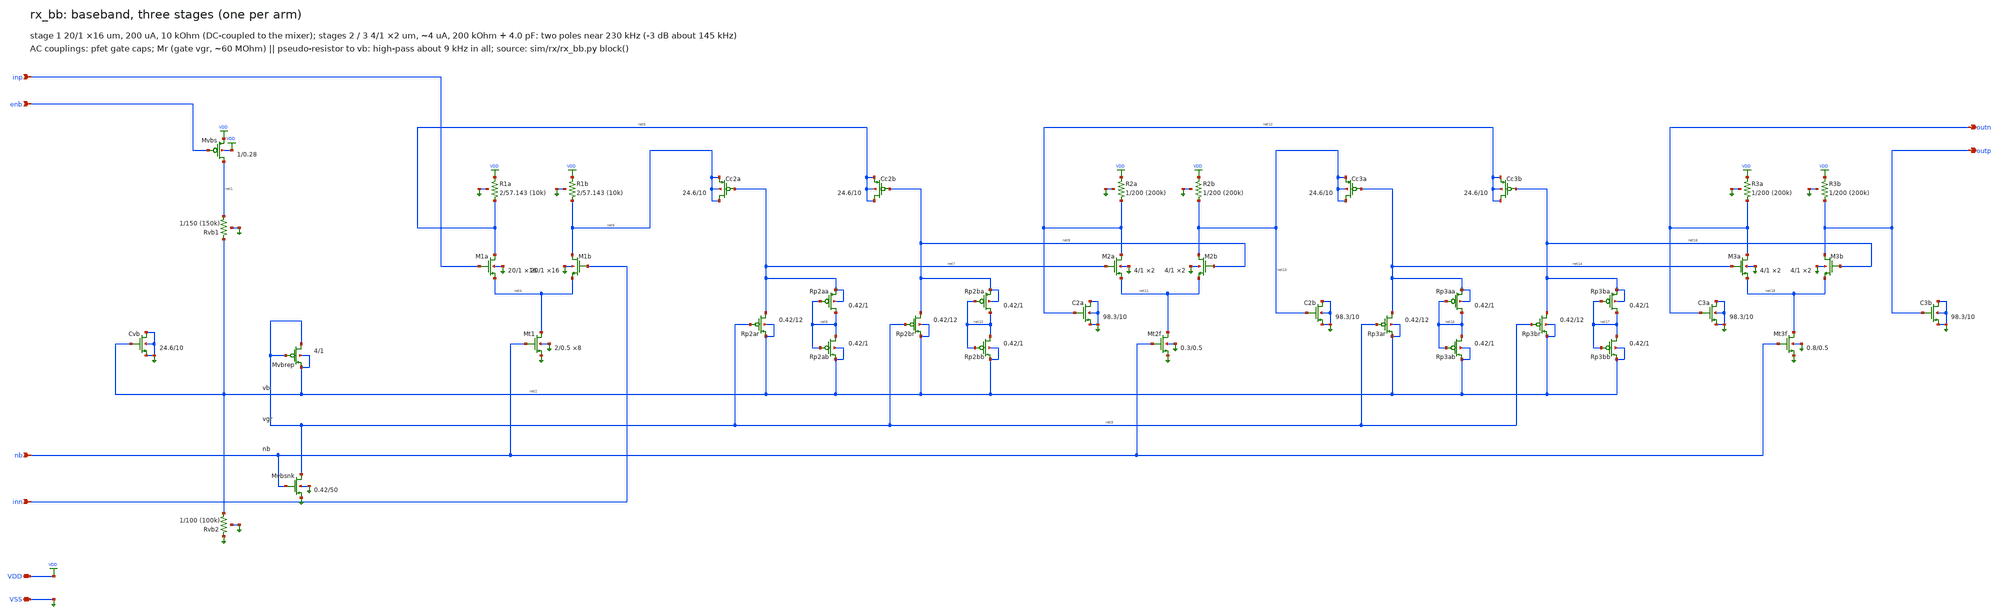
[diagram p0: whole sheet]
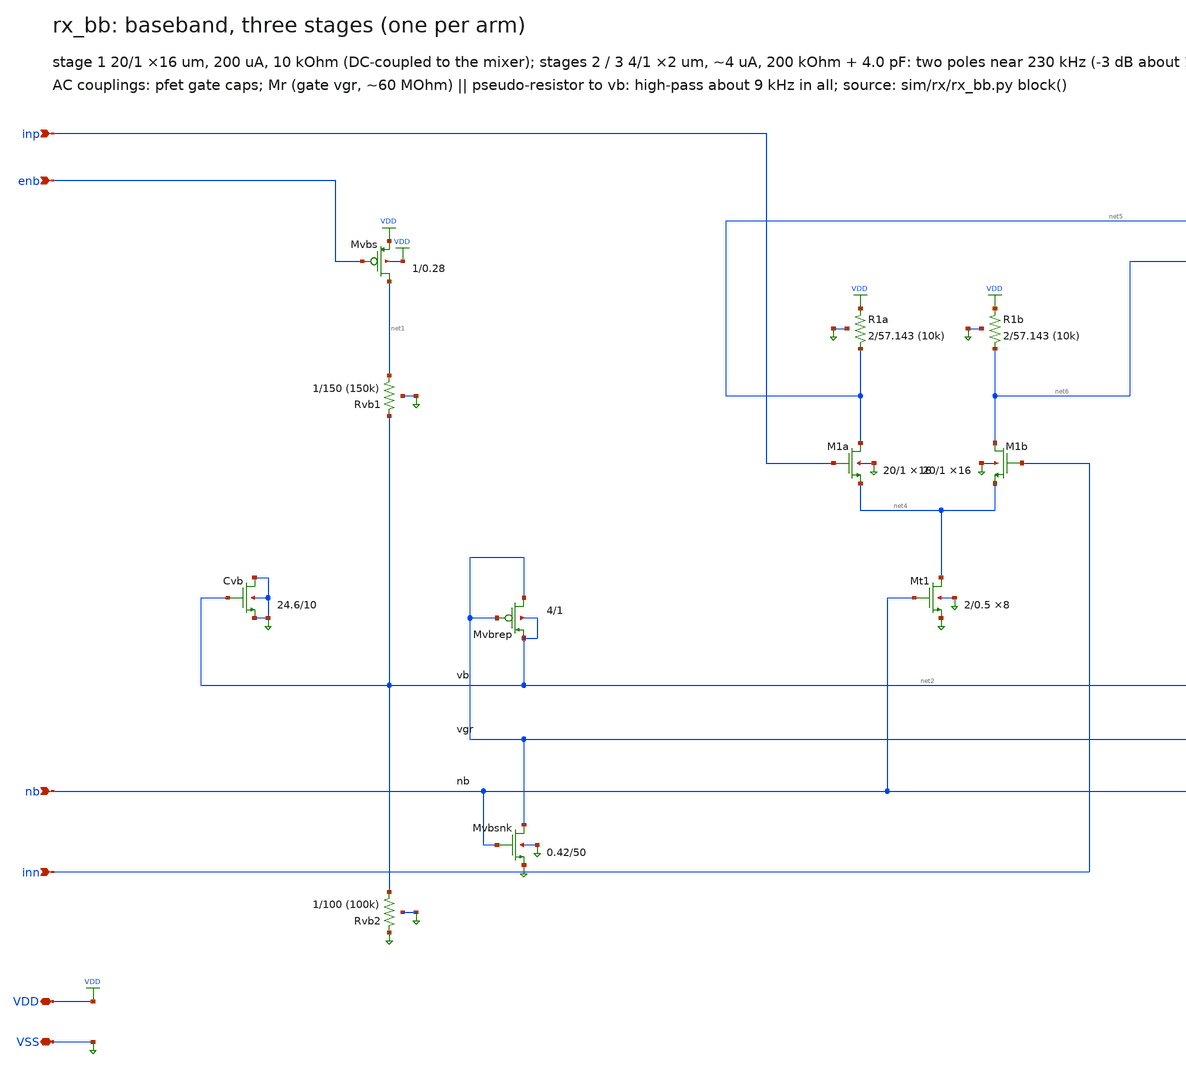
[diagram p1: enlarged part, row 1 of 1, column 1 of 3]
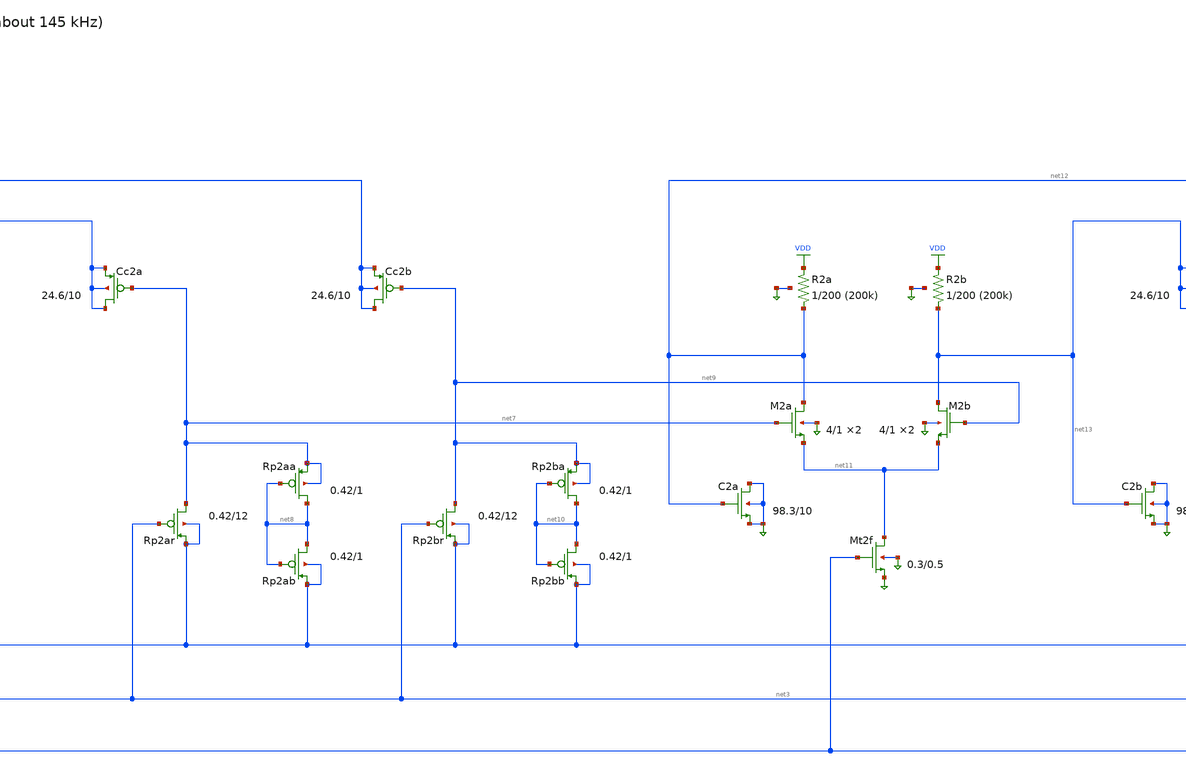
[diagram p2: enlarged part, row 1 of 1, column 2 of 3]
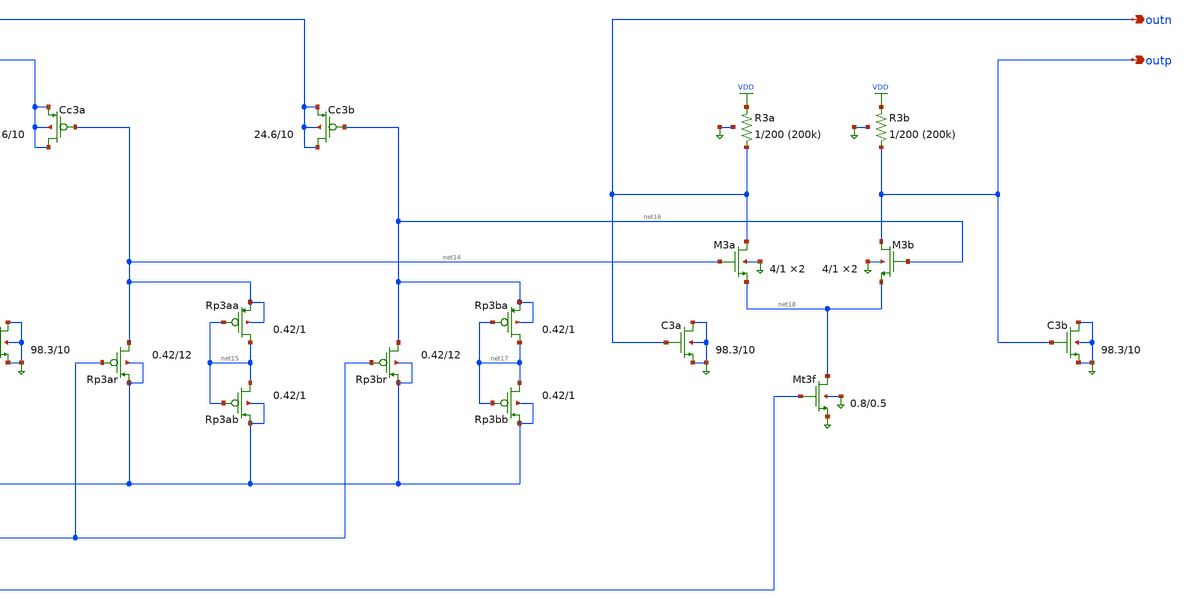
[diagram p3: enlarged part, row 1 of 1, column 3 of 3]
** sch_path: xschem/rx_bb.sch
**.subckt rx_bb VDD VSS inp inn outp outn nb enb
*.iopin VDD
*.iopin VSS
*.ipin inp
*.ipin inn
*.opin outp
*.opin outn
*.ipin nb
*.ipin enb
XMvbs net1 enb VDD VDD pfet_03v3 L=0.28u W=1.0u nf=1 ad=0.5p as=0.5p pd=3.0u ps=3.0u nrd=0 nrs=0
+ sa=0 sb=0 sd=0 m=1
XRvb1 net1 net2 VSS ppolyf_u_1k r_width=1.0e-6 r_length=150.0e-6 m=1
XRvb2 net2 VSS VSS ppolyf_u_1k r_width=1.0e-6 r_length=100.0e-6 m=1
XCvb VSS net2 VSS VSS nfet_03v3 L=10.0u W=24.57u nf=1 ad=12.285p as=12.285p pd=50.14u ps=50.14u
+ nrd=0 nrs=0 sa=0 sb=0 sd=0 m=1
XMvbrep net3 net3 net2 net2 pfet_03v3 L=1.0u W=4.0u nf=1 ad=2.0p as=2.0p pd=9.0u ps=9.0u nrd=0 nrs=0
+ sa=0 sb=0 sd=0 m=1
XMvbsnk net3 nb VSS VSS nfet_03v3 L=49.99999999999999u W=0.41999999999999993u nf=1
+ ad=0.20999999999999996p as=0.20999999999999996p pd=1.8399999999999999u ps=1.8399999999999999u nrd=0 nrs=0 sa=0 sb=0 sd=0
+ m=1
XM1a net5 inp net4 VSS nfet_03v3 L=1.0u W=20.0u nf=1 ad=10.0p as=10.0p pd=41.0u ps=41.0u nrd=0 nrs=0
+ sa=0 sb=0 sd=0 m=16
XM1b net6 inn net4 VSS nfet_03v3 L=1.0u W=20.0u nf=1 ad=10.0p as=10.0p pd=41.0u ps=41.0u nrd=0 nrs=0
+ sa=0 sb=0 sd=0 m=16
XMt1 net4 nb VSS VSS nfet_03v3 L=0.5u W=2.0u nf=1 ad=1.0p as=1.0p pd=5.0u ps=5.0u nrd=0 nrs=0 sa=0
+ sb=0 sd=0 m=8
XR1a net5 VDD VSS ppolyf_u r_width=2.0e-6 r_length=57.143e-6 m=1
XR1b net6 VDD VSS ppolyf_u r_width=2.0e-6 r_length=57.143e-6 m=1
XCc2a net6 net7 net6 net6 pfet_03v3 L=10.0u W=24.57u nf=1 ad=12.285p as=12.285p pd=50.14u ps=50.14u
+ nrd=0 nrs=0 sa=0 sb=0 sd=0 m=1
XRp2ar net7 net3 net2 net2 pfet_03v3 L=12.0u W=0.41999999999999993u nf=1 ad=0.20999999999999996p
+ as=0.20999999999999996p pd=1.8399999999999999u ps=1.8399999999999999u nrd=0 nrs=0 sa=0 sb=0 sd=0 m=1
XRp2aa net8 net8 net7 net7 pfet_03v3 L=1.0u W=0.41999999999999993u nf=1 ad=0.20999999999999996p
+ as=0.20999999999999996p pd=1.8399999999999999u ps=1.8399999999999999u nrd=0 nrs=0 sa=0 sb=0 sd=0 m=1
XRp2ab net8 net8 net2 net2 pfet_03v3 L=1.0u W=0.41999999999999993u nf=1 ad=0.20999999999999996p
+ as=0.20999999999999996p pd=1.8399999999999999u ps=1.8399999999999999u nrd=0 nrs=0 sa=0 sb=0 sd=0 m=1
XCc2b net5 net9 net5 net5 pfet_03v3 L=10.0u W=24.57u nf=1 ad=12.285p as=12.285p pd=50.14u ps=50.14u
+ nrd=0 nrs=0 sa=0 sb=0 sd=0 m=1
XRp2br net9 net3 net2 net2 pfet_03v3 L=12.0u W=0.41999999999999993u nf=1 ad=0.20999999999999996p
+ as=0.20999999999999996p pd=1.8399999999999999u ps=1.8399999999999999u nrd=0 nrs=0 sa=0 sb=0 sd=0 m=1
XRp2ba net10 net10 net9 net9 pfet_03v3 L=1.0u W=0.41999999999999993u nf=1 ad=0.20999999999999996p
+ as=0.20999999999999996p pd=1.8399999999999999u ps=1.8399999999999999u nrd=0 nrs=0 sa=0 sb=0 sd=0 m=1
XRp2bb net10 net10 net2 net2 pfet_03v3 L=1.0u W=0.41999999999999993u nf=1 ad=0.20999999999999996p
+ as=0.20999999999999996p pd=1.8399999999999999u ps=1.8399999999999999u nrd=0 nrs=0 sa=0 sb=0 sd=0 m=1
XM2a net12 net7 net11 VSS nfet_03v3 L=1.0u W=4.0u nf=1 ad=2.0p as=2.0p pd=9.0u ps=9.0u nrd=0 nrs=0
+ sa=0 sb=0 sd=0 m=2
XM2b net13 net9 net11 VSS nfet_03v3 L=1.0u W=4.0u nf=1 ad=2.0p as=2.0p pd=9.0u ps=9.0u nrd=0 nrs=0
+ sa=0 sb=0 sd=0 m=2
XMt2f net11 nb VSS VSS nfet_03v3 L=0.5u W=0.3u nf=1 ad=0.15p as=0.15p pd=1.6u ps=1.6u nrd=0 nrs=0
+ sa=0 sb=0 sd=0 m=1
XR2a net12 VDD VSS ppolyf_u_1k r_width=1.0e-6 r_length=200.0e-6 m=1
XR2b net13 VDD VSS ppolyf_u_1k r_width=1.0e-6 r_length=200.0e-6 m=1
XC2a VSS net12 VSS VSS nfet_03v3 L=10.0u W=98.28009999999999u nf=1 ad=49.140049999999995p
+ as=49.140049999999995p pd=197.56019999999998u ps=197.56019999999998u nrd=0 nrs=0 sa=0 sb=0 sd=0 m=1
XC2b VSS net13 VSS VSS nfet_03v3 L=10.0u W=98.28009999999999u nf=1 ad=49.140049999999995p
+ as=49.140049999999995p pd=197.56019999999998u ps=197.56019999999998u nrd=0 nrs=0 sa=0 sb=0 sd=0 m=1
XCc3a net13 net14 net13 net13 pfet_03v3 L=10.0u W=24.57u nf=1 ad=12.285p as=12.285p pd=50.14u
+ ps=50.14u nrd=0 nrs=0 sa=0 sb=0 sd=0 m=1
XRp3ar net14 net3 net2 net2 pfet_03v3 L=12.0u W=0.41999999999999993u nf=1 ad=0.20999999999999996p
+ as=0.20999999999999996p pd=1.8399999999999999u ps=1.8399999999999999u nrd=0 nrs=0 sa=0 sb=0 sd=0 m=1
XRp3aa net15 net15 net14 net14 pfet_03v3 L=1.0u W=0.41999999999999993u nf=1 ad=0.20999999999999996p
+ as=0.20999999999999996p pd=1.8399999999999999u ps=1.8399999999999999u nrd=0 nrs=0 sa=0 sb=0 sd=0 m=1
XRp3ab net15 net15 net2 net2 pfet_03v3 L=1.0u W=0.41999999999999993u nf=1 ad=0.20999999999999996p
+ as=0.20999999999999996p pd=1.8399999999999999u ps=1.8399999999999999u nrd=0 nrs=0 sa=0 sb=0 sd=0 m=1
XCc3b net12 net16 net12 net12 pfet_03v3 L=10.0u W=24.57u nf=1 ad=12.285p as=12.285p pd=50.14u
+ ps=50.14u nrd=0 nrs=0 sa=0 sb=0 sd=0 m=1
XRp3br net16 net3 net2 net2 pfet_03v3 L=12.0u W=0.41999999999999993u nf=1 ad=0.20999999999999996p
+ as=0.20999999999999996p pd=1.8399999999999999u ps=1.8399999999999999u nrd=0 nrs=0 sa=0 sb=0 sd=0 m=1
XRp3ba net17 net17 net16 net16 pfet_03v3 L=1.0u W=0.41999999999999993u nf=1 ad=0.20999999999999996p
+ as=0.20999999999999996p pd=1.8399999999999999u ps=1.8399999999999999u nrd=0 nrs=0 sa=0 sb=0 sd=0 m=1
XRp3bb net17 net17 net2 net2 pfet_03v3 L=1.0u W=0.41999999999999993u nf=1 ad=0.20999999999999996p
+ as=0.20999999999999996p pd=1.8399999999999999u ps=1.8399999999999999u nrd=0 nrs=0 sa=0 sb=0 sd=0 m=1
XM3a outn net14 net18 VSS nfet_03v3 L=1.0u W=4.0u nf=1 ad=2.0p as=2.0p pd=9.0u ps=9.0u nrd=0 nrs=0
+ sa=0 sb=0 sd=0 m=2
XM3b outp net16 net18 VSS nfet_03v3 L=1.0u W=4.0u nf=1 ad=2.0p as=2.0p pd=9.0u ps=9.0u nrd=0 nrs=0
+ sa=0 sb=0 sd=0 m=2
XMt3f net18 nb VSS VSS nfet_03v3 L=0.5u W=0.7999999999999999u nf=1 ad=0.39999999999999997p
+ as=0.39999999999999997p pd=2.5999999999999996u ps=2.5999999999999996u nrd=0 nrs=0 sa=0 sb=0 sd=0 m=1
XR3a outn VDD VSS ppolyf_u_1k r_width=1.0e-6 r_length=200.0e-6 m=1
XR3b outp VDD VSS ppolyf_u_1k r_width=1.0e-6 r_length=200.0e-6 m=1
XC3a VSS outn VSS VSS nfet_03v3 L=10.0u W=98.28009999999999u nf=1 ad=49.140049999999995p
+ as=49.140049999999995p pd=197.56019999999998u ps=197.56019999999998u nrd=0 nrs=0 sa=0 sb=0 sd=0 m=1
XC3b VSS outp VSS VSS nfet_03v3 L=10.0u W=98.28009999999999u nf=1 ad=49.140049999999995p
+ as=49.140049999999995p pd=197.56019999999998u ps=197.56019999999998u nrd=0 nrs=0 sa=0 sb=0 sd=0 m=1
**.ends
.end
